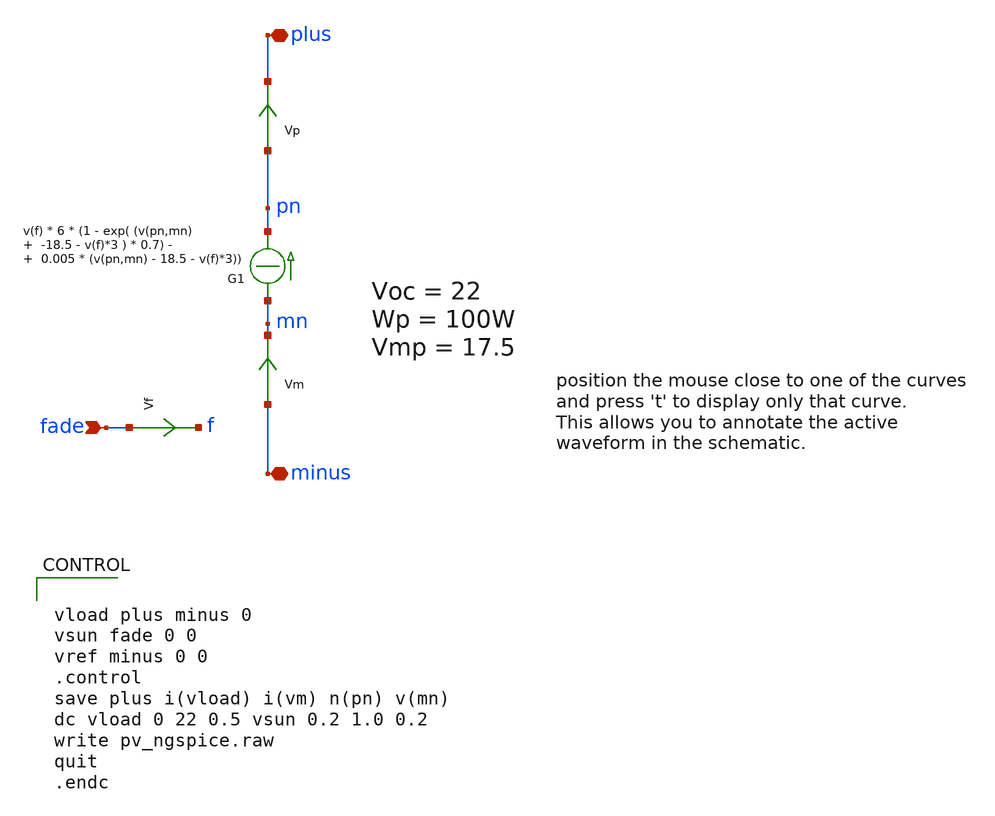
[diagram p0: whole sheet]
** sch_path: xschem_library/ngspice/pv_ngspice.sch
**.subckt pv_ngspice plus minus fade
*.iopin plus
*.iopin minus
*.ipin fade
Vm minus mn 0
.save i(vm)
G1 mn pn CUR=' v(f) * 6 * (1 - exp( (v(pn,mn) -18.5 - v(f)*3 ) * 0.7) - 0.005 * (v(pn,mn) - 18.5 - v(f)*3)) '
Vf fade f 0
.save i(vf)
Vp pn plus 0
.save i(vp)
**** begin user architecture code


vload plus minus 0
vsun fade 0 0
vref minus 0 0
.control
save plus i(vload) i(vm) n(pn) v(mn)
dc vload 0 22 0.5 vsun 0.2 1.0 0.2
write pv_ngspice.raw
quit
.endc


**** end user architecture code
**.ends
.end
